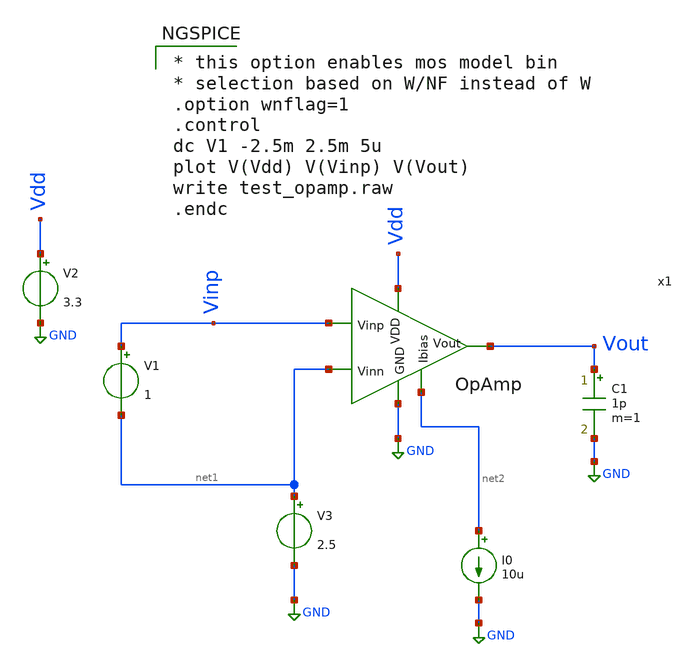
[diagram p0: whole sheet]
** sch_path: xschem/OpAmp_v0/oa_openloop_tb.sch
**.subckt oa_openloop_tb
V2 Vdd GND 3.3
I0 net2 GND 10u
x1 Vdd Vout net2 net1 Vinp GND OpAmp
C1 Vout GND 1p m=1
V1 Vinp net1 1
V3 net1 GND 2.5
**** begin user architecture code

* this option enables mos model bin
* selection based on W/NF instead of W
.option wnflag=1
.control
dc V1 -2.5m 2.5m 5u
plot V(Vdd) V(Vinp) V(Vout)
write test_opamp.raw
.endc


.lib /foss/designs/PDK/sky130B/libs.tech/ngspice/sky130.lib.spice tt
.include /foss/designs/PDK/sky130B/libs.ref/sky130_fd_sc_hvl/spice/sky130_fd_sc_hvl.spice

**** end user architecture code
**.ends
.GLOBAL GND
.end
